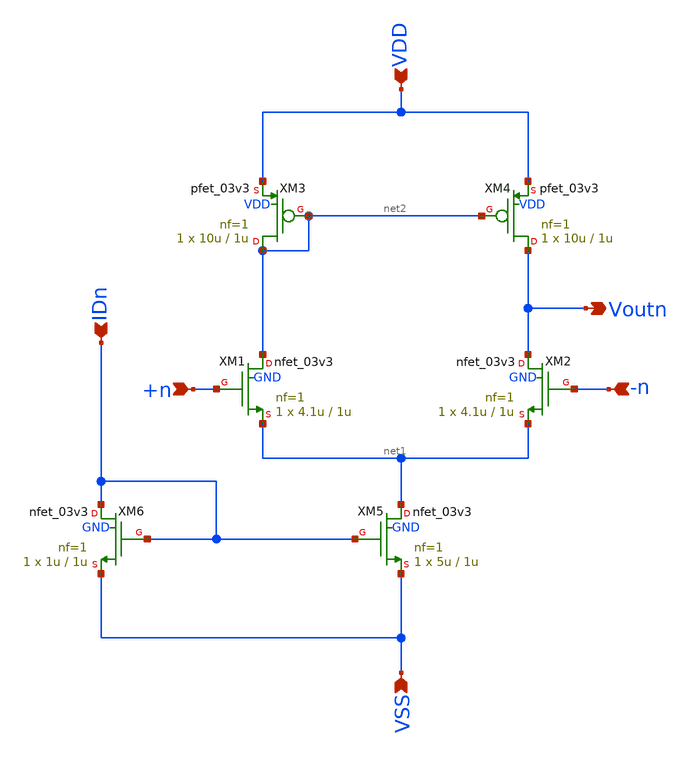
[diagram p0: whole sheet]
** sch_path: xschem/ota_miller/ota_n_in.sch
**.subckt ota_n_in Voutn VSS VDD +n -n IDn
*.opin Voutn
*.ipin VSS
*.ipin VDD
*.ipin +n
*.ipin -n
*.ipin IDn
XM1 net2 +n net1 GND nfet_03v3 L=1u W=4.1u nf=1 ad='int((nf+1)/2) * W/nf * 0.18u' as='int((nf+2)/2) * W/nf * 0.18u'
+ pd='2*int((nf+1)/2) * (W/nf + 0.18u)' ps='2*int((nf+2)/2) * (W/nf + 0.18u)' nrd='0.18u / W' nrs='0.18u / W'
+ sa=0 sb=0 sd=0 m=1 par=1
XM2 Voutn -n net1 GND nfet_03v3 L=1u W=4.1u nf=1 ad='int((nf+1)/2) * W/nf * 0.18u' as='int((nf+2)/2) * W/nf * 0.18u'
+ pd='2*int((nf+1)/2) * (W/nf + 0.18u)' ps='2*int((nf+2)/2) * (W/nf + 0.18u)' nrd='0.18u / W' nrs='0.18u / W'
+ sa=0 sb=0 sd=0 m=1 par=1
XM3 net2 net2 VDD VDD pfet_03v3 L=1u W=10u nf=1 ad='int((nf+1)/2) * W/nf * 0.18u' as='int((nf+2)/2) * W/nf * 0.18u'
+ pd='2*int((nf+1)/2) * (W/nf + 0.18u)' ps='2*int((nf+2)/2) * (W/nf + 0.18u)' nrd='0.18u / W' nrs='0.18u / W'
+ sa=0 sb=0 sd=0 m=1 par=1
XM4 Voutn net2 VDD VDD pfet_03v3 L=1u W=10u nf=1 ad='int((nf+1)/2) * W/nf * 0.18u' as='int((nf+2)/2) * W/nf * 0.18u'
+ pd='2*int((nf+1)/2) * (W/nf + 0.18u)' ps='2*int((nf+2)/2) * (W/nf + 0.18u)' nrd='0.18u / W' nrs='0.18u / W'
+ sa=0 sb=0 sd=0 m=1 par=1
XM5 net1 IDn VSS GND nfet_03v3 L=1u W=5u nf=1 ad='int((nf+1)/2) * W/nf * 0.18u' as='int((nf+2)/2) * W/nf * 0.18u'
+ pd='2*int((nf+1)/2) * (W/nf + 0.18u)' ps='2*int((nf+2)/2) * (W/nf + 0.18u)' nrd='0.18u / W' nrs='0.18u / W'
+ sa=0 sb=0 sd=0 m=1 par=1
XM6 IDn IDn VSS GND nfet_03v3 L=1u W=1u nf=1 ad='int((nf+1)/2) * W/nf * 0.18u' as='int((nf+2)/2) * W/nf * 0.18u'
+ pd='2*int((nf+1)/2) * (W/nf + 0.18u)' ps='2*int((nf+2)/2) * (W/nf + 0.18u)' nrd='0.18u / W' nrs='0.18u / W'
+ sa=0 sb=0 sd=0 m=1 par=1
**.ends
.end
